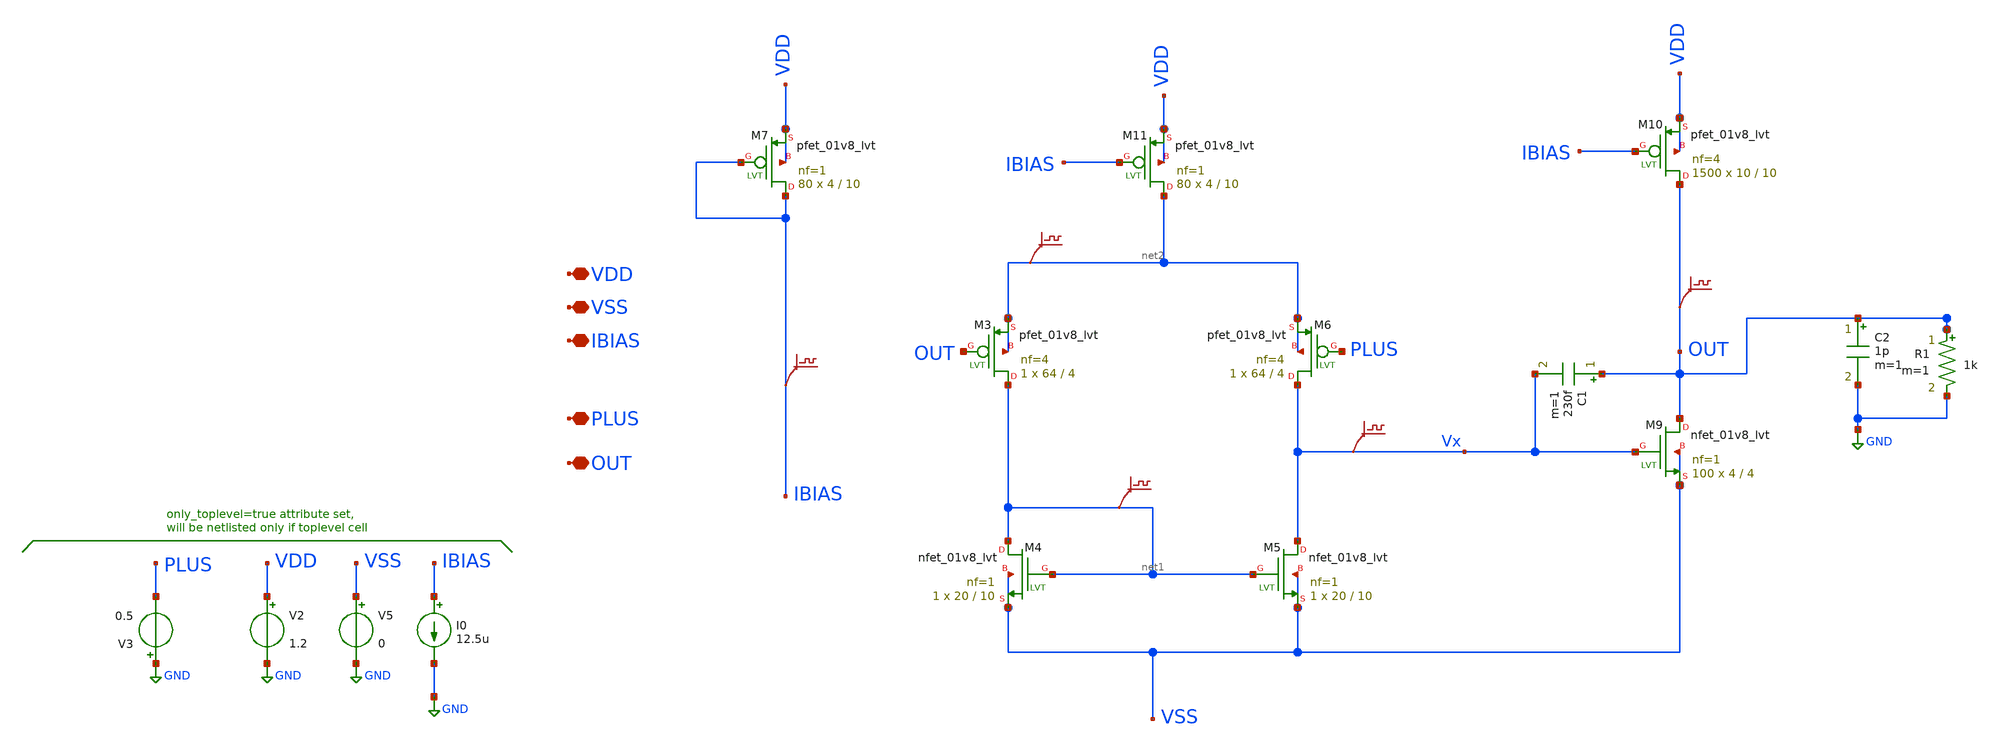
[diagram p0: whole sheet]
** sch_path: q2_opamp_settling_0.8patlama.sch
**.subckt q2_opamp_settling_0.8patlama VDD VSS PLUS OUT IBIAS
*.iopin VDD
*.iopin VSS
*.iopin PLUS
*.iopin OUT
*.iopin IBIAS
V5 VSS GND 0
I0 IBIAS GND 12.5u
V2 VDD GND 1.2
.save v(vx)
XM4 net1 net1 VSS VSS sky130_fd_pr__nfet_01v8_lvt L=10 W=20 nf=1 ad='int((nf+1)/2) * W/nf * 0.29' as='int((nf+2)/2) * W/nf * 0.29'
+ pd='2*int((nf+1)/2) * (W/nf + 0.29)' ps='2*int((nf+2)/2) * (W/nf + 0.29)' nrd='0.29 / W' nrs='0.29 / W'
+ sa=0 sb=0 sd=0 mult=1 m=1
XM5 Vx net1 VSS VSS sky130_fd_pr__nfet_01v8_lvt L=10 W=20 nf=1 ad='int((nf+1)/2) * W/nf * 0.29' as='int((nf+2)/2) * W/nf * 0.29'
+ pd='2*int((nf+1)/2) * (W/nf + 0.29)' ps='2*int((nf+2)/2) * (W/nf + 0.29)' nrd='0.29 / W' nrs='0.29 / W'
+ sa=0 sb=0 sd=0 mult=1 m=1
XM3 net1 OUT net2 net2 sky130_fd_pr__pfet_01v8_lvt L=4 W=64 nf=4 ad='int((nf+1)/2) * W/nf * 0.29' as='int((nf+2)/2) * W/nf * 0.29'
+ pd='2*int((nf+1)/2) * (W/nf + 0.29)' ps='2*int((nf+2)/2) * (W/nf + 0.29)' nrd='0.29 / W' nrs='0.29 / W'
+ sa=0 sb=0 sd=0 mult=1 m=1
XM6 Vx PLUS net2 net2 sky130_fd_pr__pfet_01v8_lvt L=4 W=64 nf=4 ad='int((nf+1)/2) * W/nf * 0.29' as='int((nf+2)/2) * W/nf * 0.29'
+ pd='2*int((nf+1)/2) * (W/nf + 0.29)' ps='2*int((nf+2)/2) * (W/nf + 0.29)' nrd='0.29 / W' nrs='0.29 / W'
+ sa=0 sb=0 sd=0 mult=1 m=1
XM7 IBIAS IBIAS VDD VDD sky130_fd_pr__pfet_01v8_lvt L=10 W=4 nf=1 ad='int((nf+1)/2) * W/nf * 0.29' as='int((nf+2)/2) * W/nf * 0.29'
+ pd='2*int((nf+1)/2) * (W/nf + 0.29)' ps='2*int((nf+2)/2) * (W/nf + 0.29)' nrd='0.29 / W' nrs='0.29 / W'
+ sa=0 sb=0 sd=0 mult=80 m=80
.save v(net2)
XM9 OUT Vx VSS VSS sky130_fd_pr__nfet_01v8_lvt L=4 W=4 nf=1 ad='int((nf+1)/2) * W/nf * 0.29' as='int((nf+2)/2) * W/nf * 0.29'
+ pd='2*int((nf+1)/2) * (W/nf + 0.29)' ps='2*int((nf+2)/2) * (W/nf + 0.29)' nrd='0.29 / W' nrs='0.29 / W'
+ sa=0 sb=0 sd=0 mult=100 m=100
XM10 OUT IBIAS VDD VDD sky130_fd_pr__pfet_01v8_lvt L=10 W=10 nf=4 ad='int((nf+1)/2) * W/nf * 0.29' as='int((nf+2)/2) * W/nf * 0.29'
+ pd='2*int((nf+1)/2) * (W/nf + 0.29)' ps='2*int((nf+2)/2) * (W/nf + 0.29)' nrd='0.29 / W' nrs='0.29 / W'
+ sa=0 sb=0 sd=0 mult=1500 m=1500
XM11 net2 IBIAS VDD VDD sky130_fd_pr__pfet_01v8_lvt L=10 W=4 nf=1 ad='int((nf+1)/2) * W/nf * 0.29' as='int((nf+2)/2) * W/nf * 0.29'
+ pd='2*int((nf+1)/2) * (W/nf + 0.29)' ps='2*int((nf+2)/2) * (W/nf + 0.29)' nrd='0.29 / W' nrs='0.29 / W'
+ sa=0 sb=0 sd=0 mult=80 m=80
.save v(net1)
.save v(out)
.save v(ibias)
C1 OUT Vx 230f m=1
C2 OUT GND 1p m=1
R1 OUT GND 1k m=1
V3 GND PLUS 0.5
**** begin user architecture code

** opencircuitdesign pdks install
.lib $::SKYWATER_MODELS/sky130.lib.spice tt





.control

*ac dec 20 1 10g
*run
*plot db(v(out)) 180*cph(v(out))/pi
*plot db(v(Vx)) 180*cph(v(Vx))/pi
*reset
dc v3 0.2 0.8 0.1
*tran 0.01n 200n
*setplot tran1


save @m.xm5.msky130_fd_pr__nfet_01v8_lvt[gm]
save @m.xm5.msky130_fd_pr__nfet_01v8_lvt[vth]
save @m.xm5.msky130_fd_pr__nfet_01v8_lvt[vdsat]
save @m.xm5.msky130_fd_pr__nfet_01v8_lvt[vds]
save @m.xm5.msky130_fd_pr__nfet_01v8_lvt[id]
save @m.xm5.msky130_fd_pr__nfet_01v8_lvt[gds]

save @m.xm6.msky130_fd_pr__pfet_01v8_lvt[gm]
save @m.xm6.msky130_fd_pr__pfet_01v8_lvt[vth]
save @m.xm6.msky130_fd_pr__pfet_01v8_lvt[vdsat]
save @m.xm6.msky130_fd_pr__pfet_01v8_lvt[vds]
save @m.xm6.msky130_fd_pr__pfet_01v8_lvt[id]
save @m.xm6.msky130_fd_pr__pfet_01v8_lvt[gds]

save @m.xm9.msky130_fd_pr__nfet_01v8_lvt[gm]
save @m.xm9.msky130_fd_pr__nfet_01v8_lvt[vth]
save @m.xm9.msky130_fd_pr__nfet_01v8_lvt[vdsat]
save @m.xm9.msky130_fd_pr__nfet_01v8_lvt[vds]
save @m.xm9.msky130_fd_pr__nfet_01v8_lvt[id]
save @m.xm9.msky130_fd_pr__nfet_01v8_lvt[gds]

save @m.xm10.msky130_fd_pr__pfet_01v8_lvt[gm]
save @m.xm10.msky130_fd_pr__pfet_01v8_lvt[vth]
save @m.xm10.msky130_fd_pr__pfet_01v8_lvt[vdsat]
save @m.xm10.msky130_fd_pr__pfet_01v8_lvt[vds]
save @m.xm10.msky130_fd_pr__pfet_01v8_lvt[id]
save @m.xm10.msky130_fd_pr__pfet_01v8_lvt[gds]

save @m.xm11.msky130_fd_pr__pfet_01v8_lvt[gm]
save @m.xm11.msky130_fd_pr__pfet_01v8_lvt[vth]
save @m.xm11.msky130_fd_pr__pfet_01v8_lvt[vdsat]
save @m.xm11.msky130_fd_pr__pfet_01v8_lvt[vds]
save @m.xm11.msky130_fd_pr__pfet_01v8_lvt[id]
save @m.xm11.msky130_fd_pr__pfet_01v8_lvt[gds]


save all
op

write q2_opamp.raw

.endc


**** end user architecture code
**.ends
.GLOBAL GND
.end
